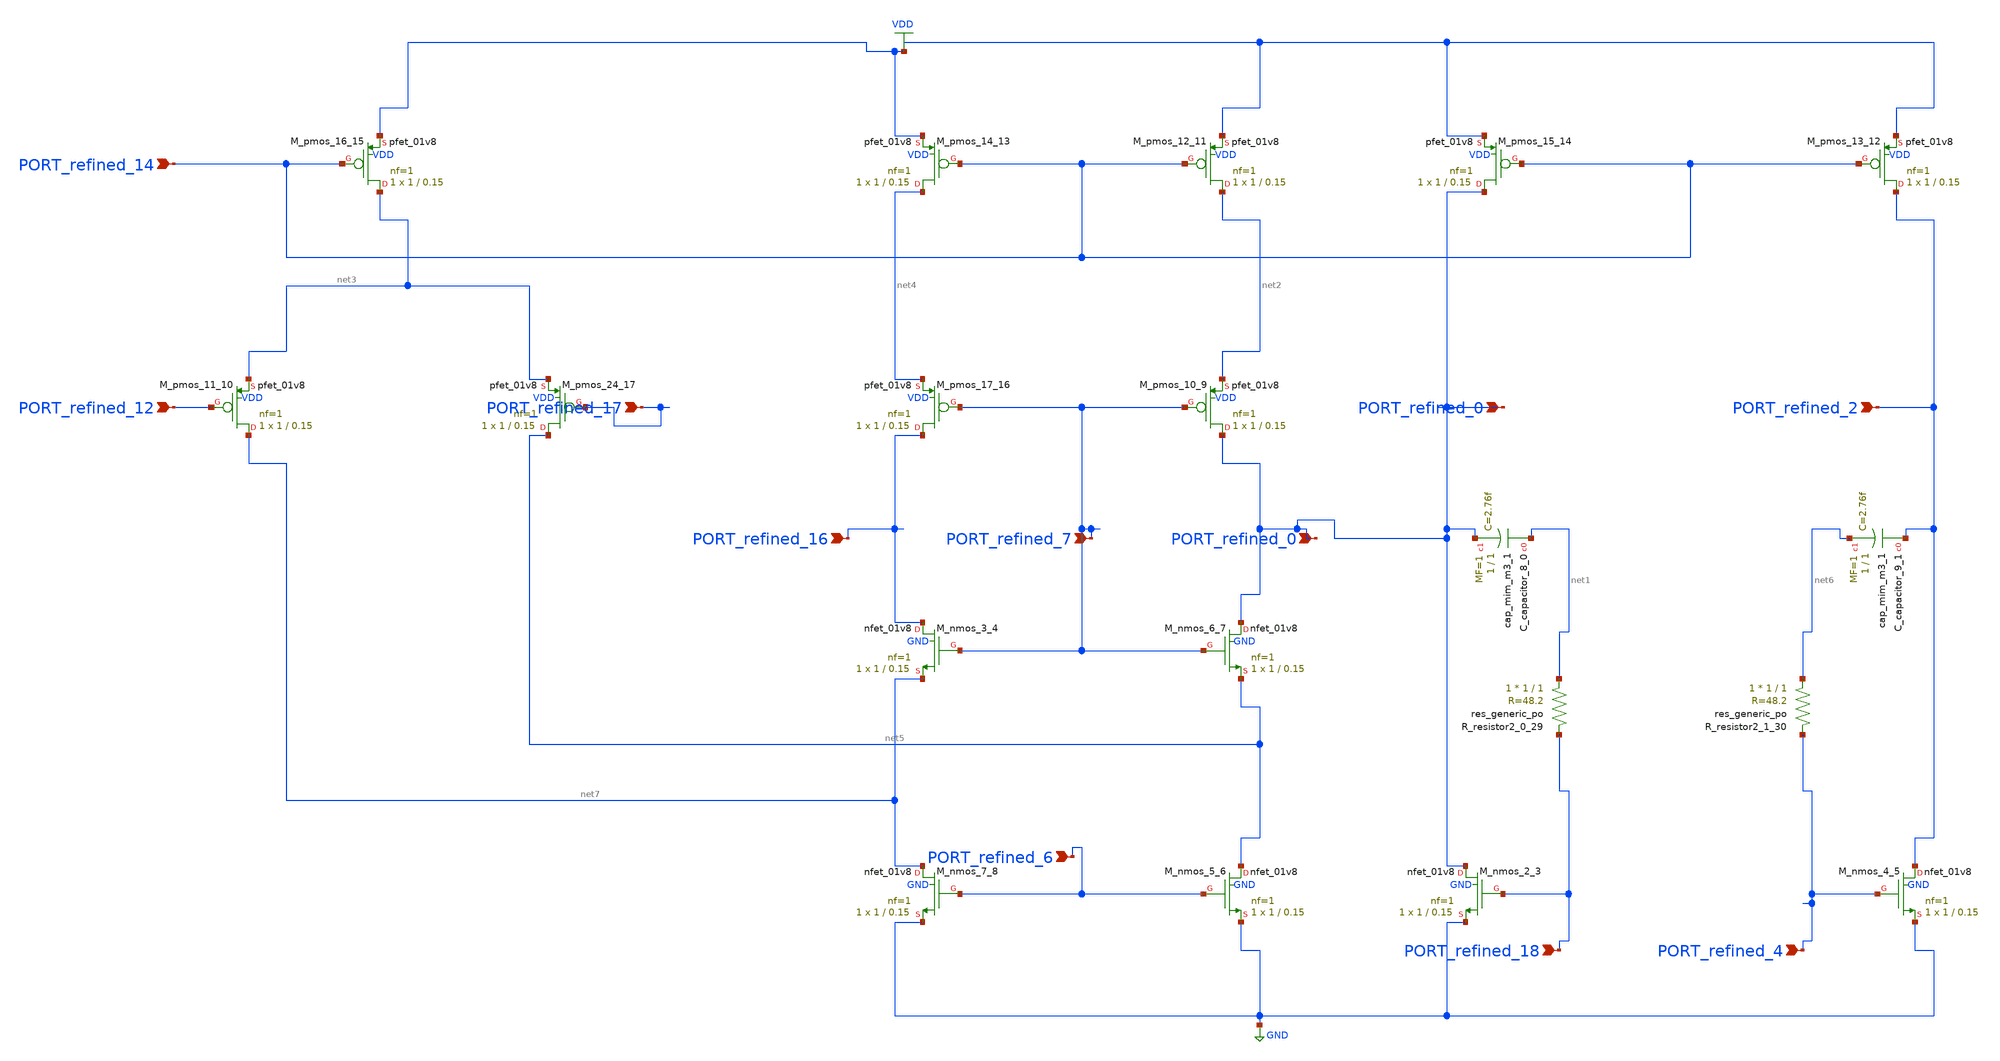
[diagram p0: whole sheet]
** sch_path: schematics/SchemGen/10_1007_s10836-016-5599-8__06_001.sch
**.subckt 10_1007_s10836-016-5599-8__06_001 PORT_refined_0 PORT_refined_12 PORT_refined_2
*+ PORT_refined_16 PORT_refined_14 PORT_refined_0 PORT_refined_6 PORT_refined_18 PORT_refined_4 PORT_refined_7
*+ PORT_refined_17
*.ipin PORT_refined_0
*.ipin PORT_refined_12
*.ipin PORT_refined_2
*.ipin PORT_refined_16
*.ipin PORT_refined_14
*.ipin PORT_refined_0
*.ipin PORT_refined_6
*.ipin PORT_refined_18
*.ipin PORT_refined_4
*.ipin PORT_refined_7
*.ipin PORT_refined_17
XC_capacitor_8_0 net1 PORT_refined_0 sky130_fd_pr__cap_mim_m3_1 W=1 L=1 MF=1 m=1
XC_capacitor_9_1 PORT_refined_2 net6 sky130_fd_pr__cap_mim_m3_1 W=1 L=1 MF=1 m=1
XM_nmos_2_3 PORT_refined_0 PORT_refined_18 GND GND sky130_fd_pr__nfet_01v8 L=0.15 W=1 nf=1 ad='int((1 + 1)/2) * 1 / 1 * 0.29'
+ as='int((1 + 2)/2) * 1 / 1 * 0.29' pd='2*int((1 + 1)/2) * (1 / 1 + 0.29)' ps='2*int((1 + 2)/2) * (1 / 1 + 0.29)'
+ nrd='0.29 / 1 ' nrs='0.29 / 1 ' sa=0 sb=0 sd=0 mult=1 m=1
XM_nmos_3_4 PORT_refined_16 PORT_refined_7 net7 GND sky130_fd_pr__nfet_01v8 L=0.15 W=1 nf=1 ad='int((1 + 1)/2) * 1 / 1 * 0.29'
+ as='int((1 + 2)/2) * 1 / 1 * 0.29' pd='2*int((1 + 1)/2) * (1 / 1 + 0.29)' ps='2*int((1 + 2)/2) * (1 / 1 + 0.29)'
+ nrd='0.29 / 1 ' nrs='0.29 / 1 ' sa=0 sb=0 sd=0 mult=1 m=1
XM_nmos_4_5 PORT_refined_2 PORT_refined_4 GND GND sky130_fd_pr__nfet_01v8 L=0.15 W=1 nf=1 ad='int((1 + 1)/2) * 1 / 1 * 0.29'
+ as='int((1 + 2)/2) * 1 / 1 * 0.29' pd='2*int((1 + 1)/2) * (1 / 1 + 0.29)' ps='2*int((1 + 2)/2) * (1 / 1 + 0.29)'
+ nrd='0.29 / 1 ' nrs='0.29 / 1 ' sa=0 sb=0 sd=0 mult=1 m=1
XM_nmos_5_6 net5 PORT_refined_6 GND GND sky130_fd_pr__nfet_01v8 L=0.15 W=1 nf=1 ad='int((1 + 1)/2) * 1 / 1 * 0.29'
+ as='int((1 + 2)/2) * 1 / 1 * 0.29' pd='2*int((1 + 1)/2) * (1 / 1 + 0.29)' ps='2*int((1 + 2)/2) * (1 / 1 + 0.29)'
+ nrd='0.29 / 1 ' nrs='0.29 / 1 ' sa=0 sb=0 sd=0 mult=1 m=1
XM_nmos_6_7 PORT_refined_0 PORT_refined_7 net5 GND sky130_fd_pr__nfet_01v8 L=0.15 W=1 nf=1 ad='int((1 + 1)/2) * 1 / 1 * 0.29'
+ as='int((1 + 2)/2) * 1 / 1 * 0.29' pd='2*int((1 + 1)/2) * (1 / 1 + 0.29)' ps='2*int((1 + 2)/2) * (1 / 1 + 0.29)'
+ nrd='0.29 / 1 ' nrs='0.29 / 1 ' sa=0 sb=0 sd=0 mult=1 m=1
XM_nmos_7_8 net7 PORT_refined_6 GND GND sky130_fd_pr__nfet_01v8 L=0.15 W=1 nf=1 ad='int((1 + 1)/2) * 1 / 1 * 0.29'
+ as='int((1 + 2)/2) * 1 / 1 * 0.29' pd='2*int((1 + 1)/2) * (1 / 1 + 0.29)' ps='2*int((1 + 2)/2) * (1 / 1 + 0.29)'
+ nrd='0.29 / 1 ' nrs='0.29 / 1 ' sa=0 sb=0 sd=0 mult=1 m=1
XM_pmos_10_9 PORT_refined_0 PORT_refined_7 net2 VDD sky130_fd_pr__pfet_01v8 L=0.15 W=1 nf=1 ad='int((1 + 1)/2) * 1 / 1 * 0.29'
+ as='int((1 + 2)/2) * 1 / 1 * 0.29' pd='2*int((1 + 1)/2) * (1 / 1 + 0.29)' ps='2*int((1 + 2)/2) * (1 / 1 + 0.29)'
+ nrd='0.29 / 1 ' nrs='0.29 / 1 ' sa=0 sb=0 sd=0 mult=1 m=1
XM_pmos_11_10 net7 PORT_refined_12 net3 VDD sky130_fd_pr__pfet_01v8 L=0.15 W=1 nf=1 ad='int((1 + 1)/2) * 1 / 1 * 0.29'
+ as='int((1 + 2)/2) * 1 / 1 * 0.29' pd='2*int((1 + 1)/2) * (1 / 1 + 0.29)' ps='2*int((1 + 2)/2) * (1 / 1 + 0.29)'
+ nrd='0.29 / 1 ' nrs='0.29 / 1 ' sa=0 sb=0 sd=0 mult=1 m=1
XM_pmos_12_11 net2 PORT_refined_14 VDD VDD sky130_fd_pr__pfet_01v8 L=0.15 W=1 nf=1 ad='int((1 + 1)/2) * 1 / 1 * 0.29'
+ as='int((1 + 2)/2) * 1 / 1 * 0.29' pd='2*int((1 + 1)/2) * (1 / 1 + 0.29)' ps='2*int((1 + 2)/2) * (1 / 1 + 0.29)'
+ nrd='0.29 / 1 ' nrs='0.29 / 1 ' sa=0 sb=0 sd=0 mult=1 m=1
XM_pmos_13_12 PORT_refined_2 PORT_refined_14 VDD VDD sky130_fd_pr__pfet_01v8 L=0.15 W=1 nf=1 ad='int((1 + 1)/2) * 1 / 1 * 0.29'
+ as='int((1 + 2)/2) * 1 / 1 * 0.29' pd='2*int((1 + 1)/2) * (1 / 1 + 0.29)' ps='2*int((1 + 2)/2) * (1 / 1 + 0.29)'
+ nrd='0.29 / 1 ' nrs='0.29 / 1 ' sa=0 sb=0 sd=0 mult=1 m=1
XM_pmos_14_13 net4 PORT_refined_14 VDD VDD sky130_fd_pr__pfet_01v8 L=0.15 W=1 nf=1 ad='int((1 + 1)/2) * 1 / 1 * 0.29'
+ as='int((1 + 2)/2) * 1 / 1 * 0.29' pd='2*int((1 + 1)/2) * (1 / 1 + 0.29)' ps='2*int((1 + 2)/2) * (1 / 1 + 0.29)'
+ nrd='0.29 / 1 ' nrs='0.29 / 1 ' sa=0 sb=0 sd=0 mult=1 m=1
XM_pmos_15_14 PORT_refined_0 PORT_refined_14 VDD VDD sky130_fd_pr__pfet_01v8 L=0.15 W=1 nf=1 ad='int((1 + 1)/2) * 1 / 1 * 0.29'
+ as='int((1 + 2)/2) * 1 / 1 * 0.29' pd='2*int((1 + 1)/2) * (1 / 1 + 0.29)' ps='2*int((1 + 2)/2) * (1 / 1 + 0.29)'
+ nrd='0.29 / 1 ' nrs='0.29 / 1 ' sa=0 sb=0 sd=0 mult=1 m=1
XM_pmos_16_15 net3 PORT_refined_14 VDD VDD sky130_fd_pr__pfet_01v8 L=0.15 W=1 nf=1 ad='int((1 + 1)/2) * 1 / 1 * 0.29'
+ as='int((1 + 2)/2) * 1 / 1 * 0.29' pd='2*int((1 + 1)/2) * (1 / 1 + 0.29)' ps='2*int((1 + 2)/2) * (1 / 1 + 0.29)'
+ nrd='0.29 / 1 ' nrs='0.29 / 1 ' sa=0 sb=0 sd=0 mult=1 m=1
XM_pmos_17_16 PORT_refined_16 PORT_refined_7 net4 VDD sky130_fd_pr__pfet_01v8 L=0.15 W=1 nf=1 ad='int((1 + 1)/2) * 1 / 1 * 0.29'
+ as='int((1 + 2)/2) * 1 / 1 * 0.29' pd='2*int((1 + 1)/2) * (1 / 1 + 0.29)' ps='2*int((1 + 2)/2) * (1 / 1 + 0.29)'
+ nrd='0.29 / 1 ' nrs='0.29 / 1 ' sa=0 sb=0 sd=0 mult=1 m=1
XM_pmos_24_17 net5 PORT_refined_17 net3 VDD sky130_fd_pr__pfet_01v8 L=0.15 W=1 nf=1 ad='int((1 + 1)/2) * 1 / 1 * 0.29'
+ as='int((1 + 2)/2) * 1 / 1 * 0.29' pd='2*int((1 + 1)/2) * (1 / 1 + 0.29)' ps='2*int((1 + 2)/2) * (1 / 1 + 0.29)'
+ nrd='0.29 / 1 ' nrs='0.29 / 1 ' sa=0 sb=0 sd=0 mult=1 m=1
XR_resistor2_0_29 net1 PORT_refined_18 sky130_fd_pr__res_generic_po W=1 L=1 m=1
XR_resistor2_1_30 net6 PORT_refined_4 sky130_fd_pr__res_generic_po W=1 L=1 m=1
**.ends
.GLOBAL GND
.GLOBAL VDD
.end
